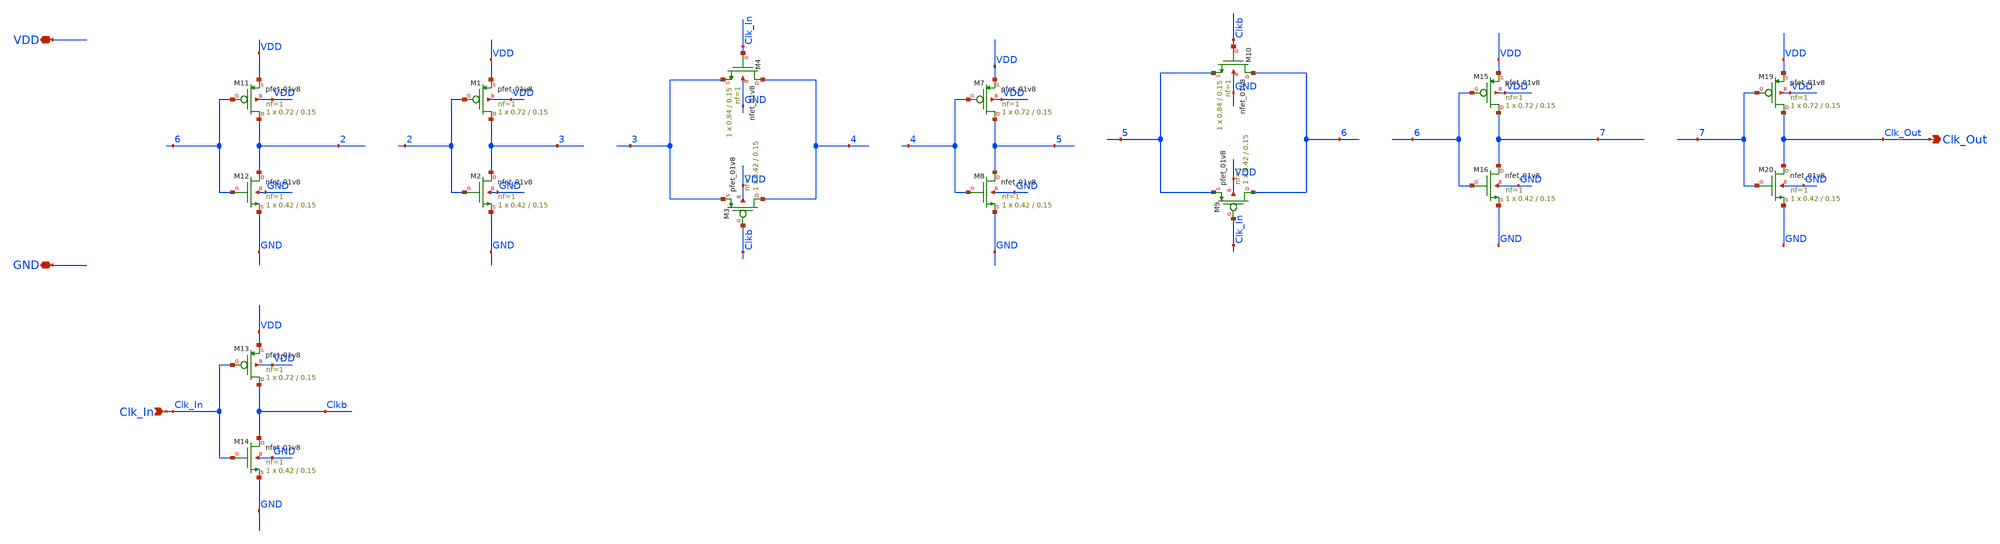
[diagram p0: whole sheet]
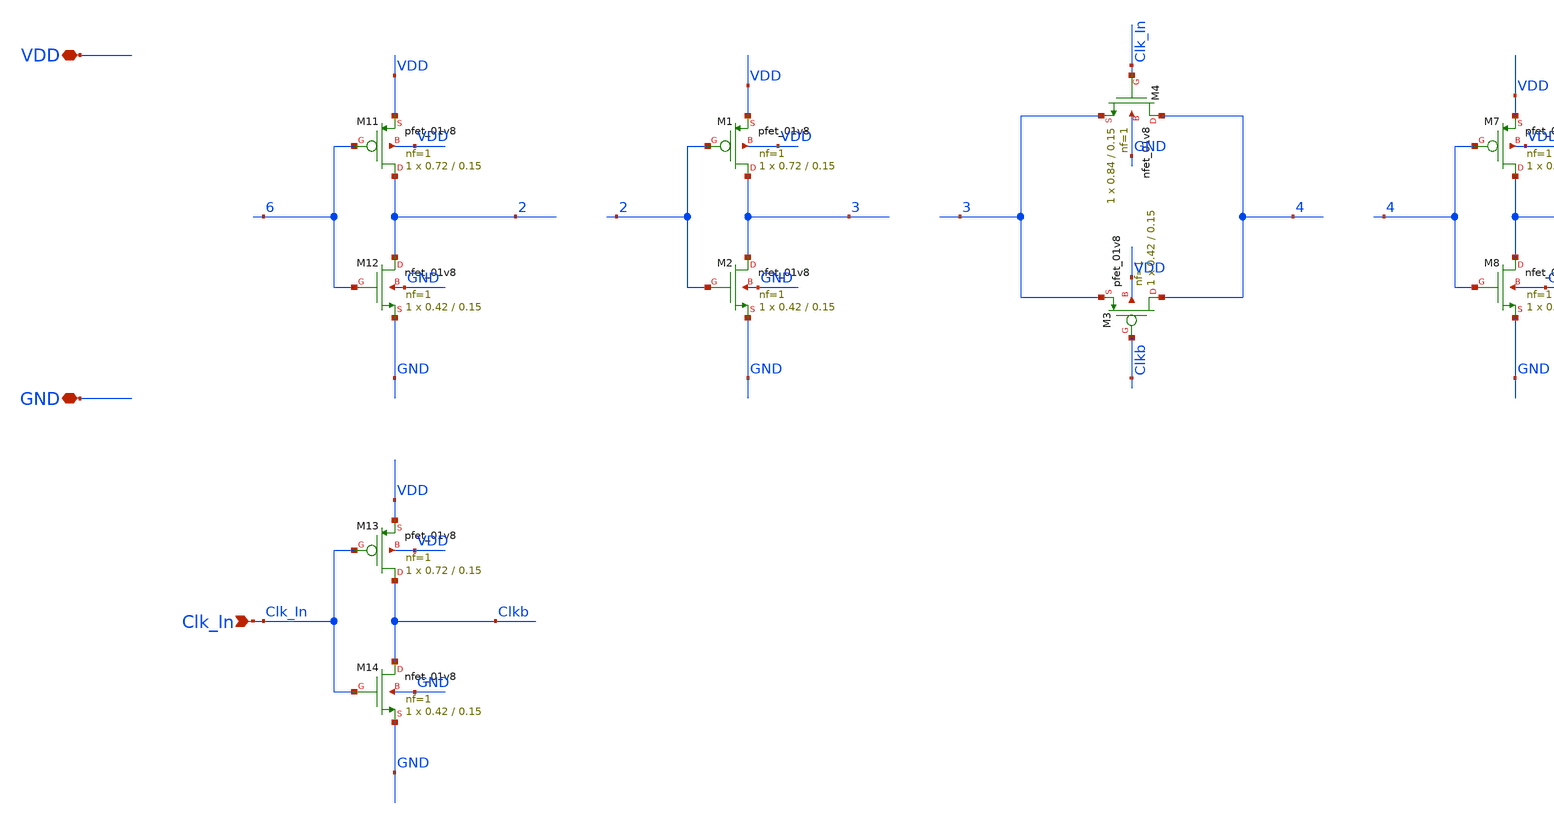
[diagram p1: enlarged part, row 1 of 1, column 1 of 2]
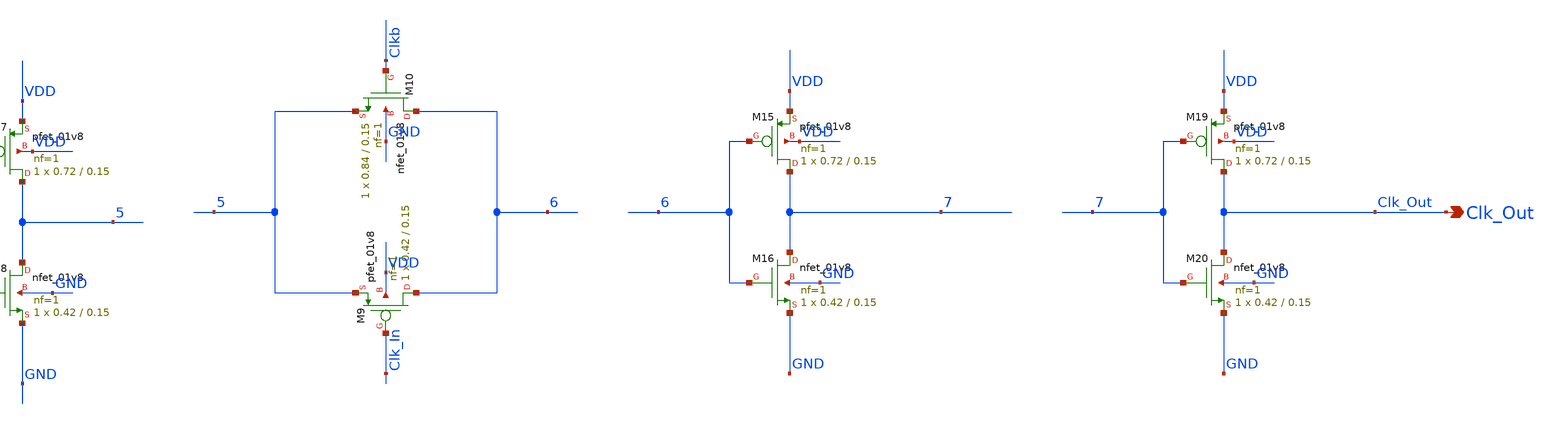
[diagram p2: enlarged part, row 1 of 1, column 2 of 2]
** sch_path: xschem/3-stage_cs-vco_dp9/FD.sch
**.subckt FD Clk_In VDD GND Clk_Out
*.ipin Clk_In
*.iopin VDD
*.iopin GND
*.opin Clk_Out
XM15 7 6 VDD VDD sky130_fd_pr__pfet_01v8 L=0.15 W=0.72 nf=1 ad='int((nf+1)/2) * W/nf * 0.29' as='int((nf+2)/2) * W/nf * 0.29'
+ pd='2*int((nf+1)/2) * (W/nf + 0.29)' ps='2*int((nf+2)/2) * (W/nf + 0.29)' nrd='0.29 / W' nrs='0.29 / W'
+ sa=0 sb=0 sd=0 mult=1 m=1
XM16 7 6 GND GND sky130_fd_pr__nfet_01v8 L=0.15 W=0.42 nf=1 ad='int((nf+1)/2) * W/nf * 0.29' as='int((nf+2)/2) * W/nf * 0.29'
+ pd='2*int((nf+1)/2) * (W/nf + 0.29)' ps='2*int((nf+2)/2) * (W/nf + 0.29)' nrd='0.29 / W' nrs='0.29 / W'
+ sa=0 sb=0 sd=0 mult=1 m=1
XM11 2 6 VDD VDD sky130_fd_pr__pfet_01v8 L=0.15 W=0.72 nf=1 ad='int((nf+1)/2) * W/nf * 0.29' as='int((nf+2)/2) * W/nf * 0.29'
+ pd='2*int((nf+1)/2) * (W/nf + 0.29)' ps='2*int((nf+2)/2) * (W/nf + 0.29)' nrd='0.29 / W' nrs='0.29 / W'
+ sa=0 sb=0 sd=0 mult=1 m=1
XM12 2 6 GND GND sky130_fd_pr__nfet_01v8 L=0.15 W=0.42 nf=1 ad='int((nf+1)/2) * W/nf * 0.29' as='int((nf+2)/2) * W/nf * 0.29'
+ pd='2*int((nf+1)/2) * (W/nf + 0.29)' ps='2*int((nf+2)/2) * (W/nf + 0.29)' nrd='0.29 / W' nrs='0.29 / W'
+ sa=0 sb=0 sd=0 mult=1 m=1
XM13 Clkb Clk_In VDD VDD sky130_fd_pr__pfet_01v8 L=0.15 W=0.72 nf=1 ad='int((nf+1)/2) * W/nf * 0.29'
+ as='int((nf+2)/2) * W/nf * 0.29' pd='2*int((nf+1)/2) * (W/nf + 0.29)' ps='2*int((nf+2)/2) * (W/nf + 0.29)'
+ nrd='0.29 / W' nrs='0.29 / W' sa=0 sb=0 sd=0 mult=1 m=1
XM14 Clkb Clk_In GND GND sky130_fd_pr__nfet_01v8 L=0.15 W=0.42 nf=1 ad='int((nf+1)/2) * W/nf * 0.29'
+ as='int((nf+2)/2) * W/nf * 0.29' pd='2*int((nf+1)/2) * (W/nf + 0.29)' ps='2*int((nf+2)/2) * (W/nf + 0.29)'
+ nrd='0.29 / W' nrs='0.29 / W' sa=0 sb=0 sd=0 mult=1 m=1
XM7 5 4 VDD VDD sky130_fd_pr__pfet_01v8 L=0.15 W=0.72 nf=1 ad='int((nf+1)/2) * W/nf * 0.29' as='int((nf+2)/2) * W/nf * 0.29'
+ pd='2*int((nf+1)/2) * (W/nf + 0.29)' ps='2*int((nf+2)/2) * (W/nf + 0.29)' nrd='0.29 / W' nrs='0.29 / W'
+ sa=0 sb=0 sd=0 mult=1 m=1
XM8 5 4 GND GND sky130_fd_pr__nfet_01v8 L=0.15 W=0.42 nf=1 ad='int((nf+1)/2) * W/nf * 0.29' as='int((nf+2)/2) * W/nf * 0.29'
+ pd='2*int((nf+1)/2) * (W/nf + 0.29)' ps='2*int((nf+2)/2) * (W/nf + 0.29)' nrd='0.29 / W' nrs='0.29 / W'
+ sa=0 sb=0 sd=0 mult=1 m=1
XM1 3 2 VDD VDD sky130_fd_pr__pfet_01v8 L=0.15 W=0.72 nf=1 ad='int((nf+1)/2) * W/nf * 0.29' as='int((nf+2)/2) * W/nf * 0.29'
+ pd='2*int((nf+1)/2) * (W/nf + 0.29)' ps='2*int((nf+2)/2) * (W/nf + 0.29)' nrd='0.29 / W' nrs='0.29 / W'
+ sa=0 sb=0 sd=0 mult=1 m=1
XM2 3 2 GND GND sky130_fd_pr__nfet_01v8 L=0.15 W=0.42 nf=1 ad='int((nf+1)/2) * W/nf * 0.29' as='int((nf+2)/2) * W/nf * 0.29'
+ pd='2*int((nf+1)/2) * (W/nf + 0.29)' ps='2*int((nf+2)/2) * (W/nf + 0.29)' nrd='0.29 / W' nrs='0.29 / W'
+ sa=0 sb=0 sd=0 mult=1 m=1
XM3 4 Clkb 3 VDD sky130_fd_pr__pfet_01v8 L=0.15 W=0.42 nf=1 ad='int((nf+1)/2) * W/nf * 0.29' as='int((nf+2)/2) * W/nf * 0.29'
+ pd='2*int((nf+1)/2) * (W/nf + 0.29)' ps='2*int((nf+2)/2) * (W/nf + 0.29)' nrd='0.29 / W' nrs='0.29 / W'
+ sa=0 sb=0 sd=0 mult=1 m=1
XM4 4 Clk_In 3 GND sky130_fd_pr__nfet_01v8 L=0.15 W=0.84 nf=1 ad='int((nf+1)/2) * W/nf * 0.29' as='int((nf+2)/2) * W/nf * 0.29'
+ pd='2*int((nf+1)/2) * (W/nf + 0.29)' ps='2*int((nf+2)/2) * (W/nf + 0.29)' nrd='0.29 / W' nrs='0.29 / W'
+ sa=0 sb=0 sd=0 mult=1 m=1
XM9 6 Clk_In 5 VDD sky130_fd_pr__pfet_01v8 L=0.15 W=0.42 nf=1 ad='int((nf+1)/2) * W/nf * 0.29' as='int((nf+2)/2) * W/nf * 0.29'
+ pd='2*int((nf+1)/2) * (W/nf + 0.29)' ps='2*int((nf+2)/2) * (W/nf + 0.29)' nrd='0.29 / W' nrs='0.29 / W'
+ sa=0 sb=0 sd=0 mult=1 m=1
XM10 6 Clkb 5 GND sky130_fd_pr__nfet_01v8 L=0.15 W=0.84 nf=1 ad='int((nf+1)/2) * W/nf * 0.29' as='int((nf+2)/2) * W/nf * 0.29'
+ pd='2*int((nf+1)/2) * (W/nf + 0.29)' ps='2*int((nf+2)/2) * (W/nf + 0.29)' nrd='0.29 / W' nrs='0.29 / W'
+ sa=0 sb=0 sd=0 mult=1 m=1
XM19 Clk_Out 7 VDD VDD sky130_fd_pr__pfet_01v8 L=0.15 W=0.72 nf=1 ad='int((nf+1)/2) * W/nf * 0.29' as='int((nf+2)/2) * W/nf * 0.29'
+ pd='2*int((nf+1)/2) * (W/nf + 0.29)' ps='2*int((nf+2)/2) * (W/nf + 0.29)' nrd='0.29 / W' nrs='0.29 / W'
+ sa=0 sb=0 sd=0 mult=1 m=1
XM20 Clk_Out 7 GND GND sky130_fd_pr__nfet_01v8 L=0.15 W=0.42 nf=1 ad='int((nf+1)/2) * W/nf * 0.29' as='int((nf+2)/2) * W/nf * 0.29'
+ pd='2*int((nf+1)/2) * (W/nf + 0.29)' ps='2*int((nf+2)/2) * (W/nf + 0.29)' nrd='0.29 / W' nrs='0.29 / W'
+ sa=0 sb=0 sd=0 mult=1 m=1
**.ends
.end
